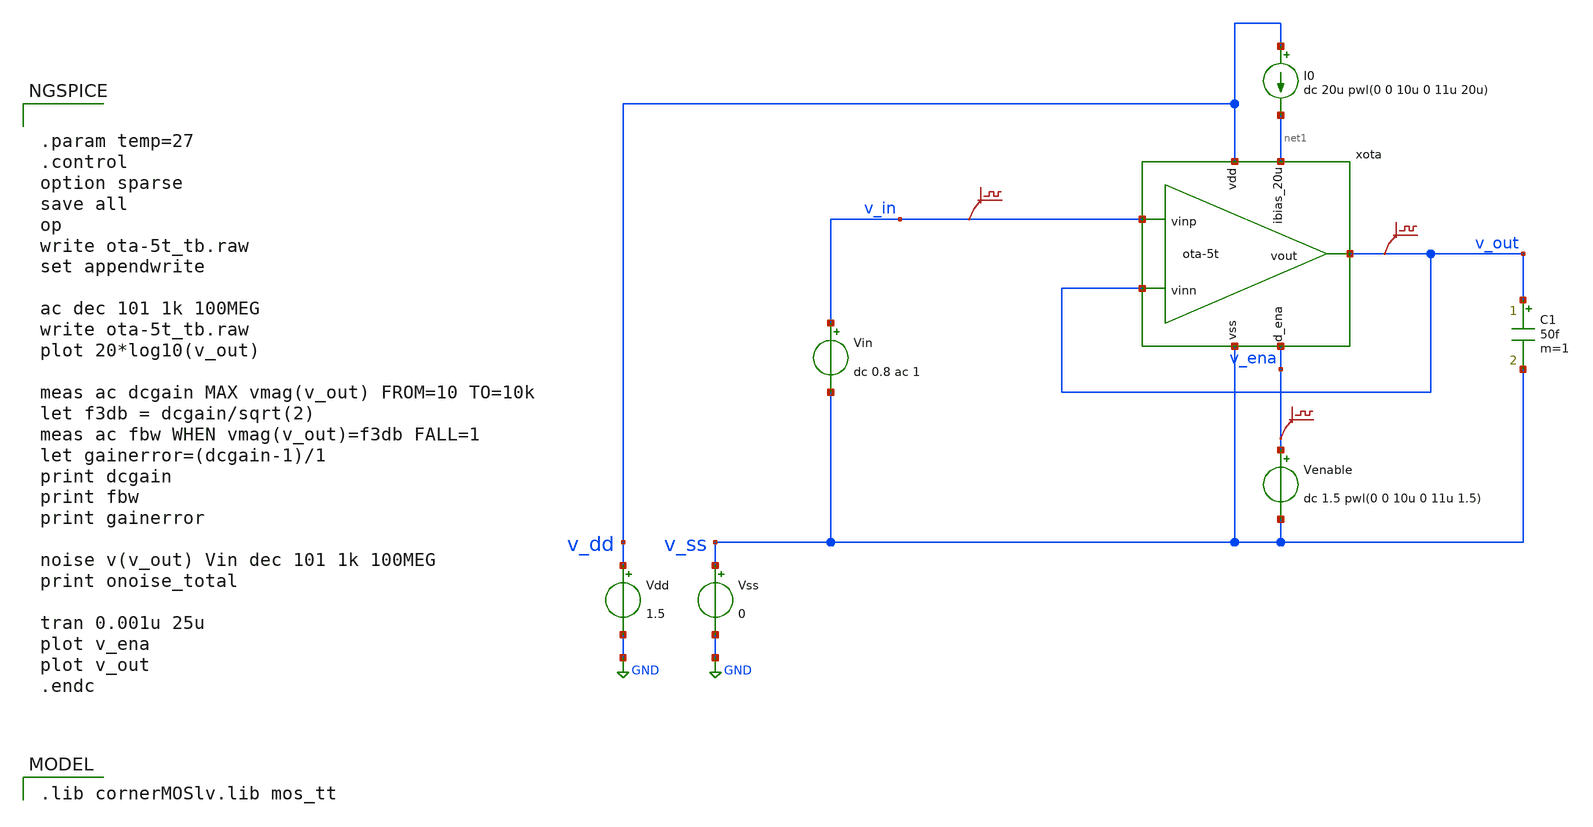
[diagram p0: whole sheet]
** sch_path: xschem/ota-5t_tb.sch
* Copyright 2024 Harald Pretl
**.subckt ota-5t_tb
Vdd v_dd GND 1.5
xota v_dd v_out v_in v_out net1 v_ena v_ss ota-5t
Vss v_ss GND 0
C1 v_out v_ss 50f m=1
Vin v_in v_ss dc 0.8 ac 1
I0 v_dd net1 dc 20u pwl(0 0 10u 0 11u 20u)
Venable v_ena v_ss dc 1.5 pwl(0 0 10u 0 11u 1.5)
.save v(v_in)
.save v(v_out)
.save v(v_ena)
**** begin user architecture code
 .lib cornerMOSlv.lib mos_tt



.param temp=27
.control
option sparse
save all
op
write ota-5t_tb.raw
set appendwrite

ac dec 101 1k 100MEG
write ota-5t_tb.raw
plot 20*log10(v_out)

meas ac dcgain MAX vmag(v_out) FROM=10 TO=10k
let f3db = dcgain/sqrt(2)
meas ac fbw WHEN vmag(v_out)=f3db FALL=1
let gainerror=(dcgain-1)/1
print dcgain
print fbw
print gainerror

noise v(v_out) Vin dec 101 1k 100MEG
print onoise_total

tran 0.001u 25u
plot v_ena
plot v_out
.endc


**** end user architecture code
**.ends

* expanding   symbol:  ota-5t.sym # of pins=7
** sym_path: xschem/ota-5t.sym
** sch_path: xschem/ota-5t.sch
.subckt ota-5t vdd vout vinp vinn ibias_20u d_ena vss
*.ipin ibias_20u
*.iopin vdd
*.iopin vss
*.ipin vinp
*.ipin vinn
*.opin vout
*.ipin d_ena
XM5 vss gate_n tail vss sg13_lv_nmos w=0.5u l=5u ng=1 m=1 mm_ok=1
XM4 vout gate_p vdd vdd sg13_lv_pmos w=1.5u l=5u ng=1 m=1 mm_ok=1
XM1 tail vinp gate_p vss sg13_lv_nmos w=2u l=5u ng=1 m=1 mm_ok=1
XM2 tail vinn vout vss sg13_lv_nmos w=2u l=5u ng=1 m=1 mm_ok=1
XM3 gate_p gate_p vdd vdd sg13_lv_pmos w=1.5u l=5u ng=1 m=1 mm_ok=1
XM6 vss gate_n ibias_20u vss sg13_lv_nmos w=2.5u l=5u ng=5 m=1 mm_ok=1
XM9 vss ena_n gate_n vss sg13_lv_nmos w=0.5u l=0.13u ng=1 m=1 mm_ok=1
XM11 gate_p d_ena vdd vdd sg13_lv_pmos w=1.5u l=0.13u ng=1 m=1 mm_ok=1
XM7 vss d_ena ena_n vss sg13_lv_nmos w=0.5u l=0.13u ng=1 m=1 mm_ok=1
XM8 ena_n d_ena vdd vdd sg13_lv_pmos w=1.5u l=0.13u ng=1 m=1 mm_ok=1
XM10 gate_n d_ena ibias_20u vss sg13_lv_nmos w=0.5u l=0.13u ng=1 m=1 mm_ok=1
.ends

.GLOBAL GND
.end
